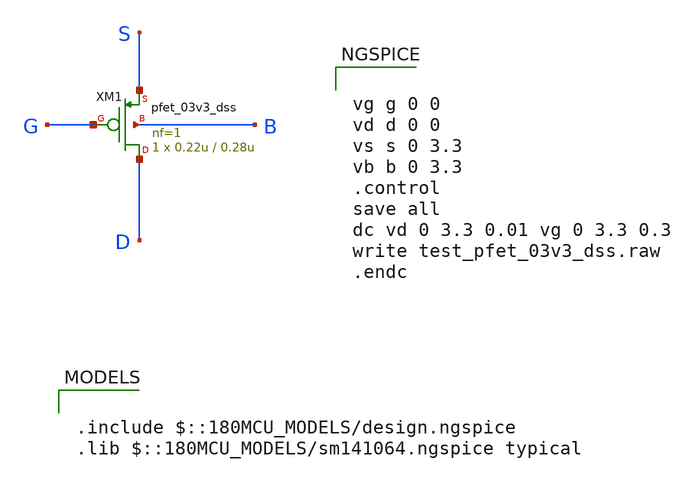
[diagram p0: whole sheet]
** sch_path: gf180mcuD/xschem_libs/gf180mcu_tests/test_pfet_03v3_dss/schematic/test_pfet_03v3_dss.sch
* Copyright 2022 GlobalFoundries PDK Authors
* Licensed under the Apache License, Version 2.0 (the "License");
* you may not use this file except in compliance with the License.
* You may obtain a copy of the License at
* https://www.apache.org/licenses/LICENSE-2.0
* Unless required by applicable law or agreed to in writing, software
* distributed under the License is distributed on an "AS IS" BASIS,
* WITHOUT WARRANTIES OR CONDITIONS OF ANY KIND, either express or implied.
* See the License for the specific language governing permissions and
* limitations under the License.
**.subckt test_pfet_03v3_dss
XM1 D G S B pfet_03v3_dss L=0.28u W=0.22u nf=1 ad='int((nf+1)/2) * W/nf * 0.18u' as='int((nf+2)/2) * W/nf * 0.18u'
+ pd='2*int((nf+1)/2) * (W/nf + 0.18u)' ps='2*int((nf+2)/2) * (W/nf + 0.18u)' nrd='0.18u / W' nrs='0.18u / W'
+ sa=0 sb=0 sd=0 d_sab=2.78u s_sab=0.28u m=1
**** begin user architecture code


vg g 0 0
vd d 0 0
vs s 0 3.3
vb b 0 3.3
.control
save all
dc vd 0 3.3 0.01 vg 0 3.3 0.3
write test_pfet_03v3_dss.raw
.endc



.include $::180MCU_MODELS/design.ngspice
.lib $::180MCU_MODELS/sm141064.ngspice typical

**** end user architecture code
**.ends
.end
